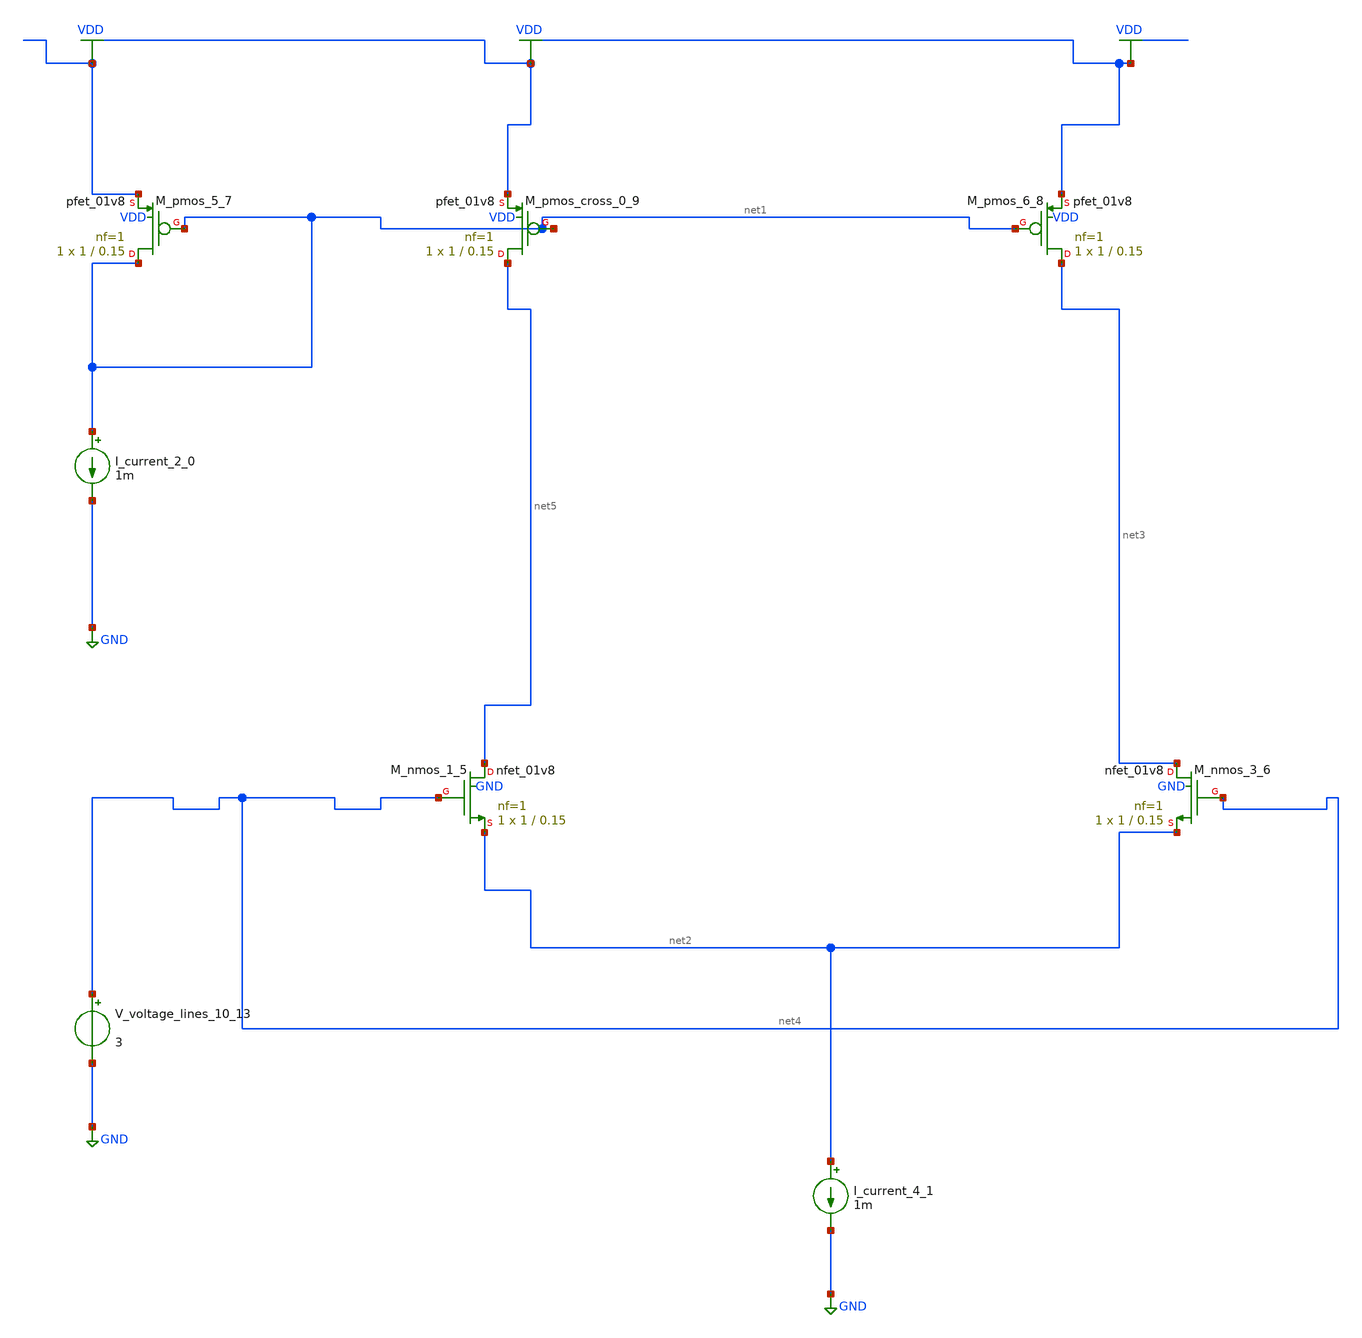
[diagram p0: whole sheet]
** sch_path: schematics/AMSNet/296.sch
**.subckt 296
I_current_2_0 net1 GND 1m
I_current_4_1 net2 GND 1m
XM_nmos_1_5 net5 net4 net2 GND sky130_fd_pr__nfet_01v8 L=0.15 W=1 nf=1 ad='int((1 + 1)/2) * 1 / 1 * 0.29'
+ as='int((1 + 2)/2) * 1 / 1 * 0.29' pd='2*int((1 + 1)/2) * (1 / 1 + 0.29)' ps='2*int((1 + 2)/2) * (1 / 1 + 0.29)'
+ nrd='0.29 / 1 ' nrs='0.29 / 1 ' sa=0 sb=0 sd=0 mult=1 m=1
XM_nmos_3_6 net3 net4 net2 GND sky130_fd_pr__nfet_01v8 L=0.15 W=1 nf=1 ad='int((1 + 1)/2) * 1 / 1 * 0.29'
+ as='int((1 + 2)/2) * 1 / 1 * 0.29' pd='2*int((1 + 1)/2) * (1 / 1 + 0.29)' ps='2*int((1 + 2)/2) * (1 / 1 + 0.29)'
+ nrd='0.29 / 1 ' nrs='0.29 / 1 ' sa=0 sb=0 sd=0 mult=1 m=1
XM_pmos_5_7 net1 net1 VDD VDD sky130_fd_pr__pfet_01v8 L=0.15 W=1 nf=1 ad='int((1 + 1)/2) * 1 / 1 * 0.29'
+ as='int((1 + 2)/2) * 1 / 1 * 0.29' pd='2*int((1 + 1)/2) * (1 / 1 + 0.29)' ps='2*int((1 + 2)/2) * (1 / 1 + 0.29)'
+ nrd='0.29 / 1 ' nrs='0.29 / 1 ' sa=0 sb=0 sd=0 mult=1 m=1
XM_pmos_6_8 net3 net1 VDD VDD sky130_fd_pr__pfet_01v8 L=0.15 W=1 nf=1 ad='int((1 + 1)/2) * 1 / 1 * 0.29'
+ as='int((1 + 2)/2) * 1 / 1 * 0.29' pd='2*int((1 + 1)/2) * (1 / 1 + 0.29)' ps='2*int((1 + 2)/2) * (1 / 1 + 0.29)'
+ nrd='0.29 / 1 ' nrs='0.29 / 1 ' sa=0 sb=0 sd=0 mult=1 m=1
XM_pmos_cross_0_9 net5 net1 VDD VDD sky130_fd_pr__pfet_01v8 L=0.15 W=1 nf=1 ad='int((1 + 1)/2) * 1 / 1 * 0.29'
+ as='int((1 + 2)/2) * 1 / 1 * 0.29' pd='2*int((1 + 1)/2) * (1 / 1 + 0.29)' ps='2*int((1 + 2)/2) * (1 / 1 + 0.29)'
+ nrd='0.29 / 1 ' nrs='0.29 / 1 ' sa=0 sb=0 sd=0 mult=1 m=1
V_voltage_lines_10_13 net4 GND 3
**.ends
.GLOBAL GND
.GLOBAL VDD
.end
